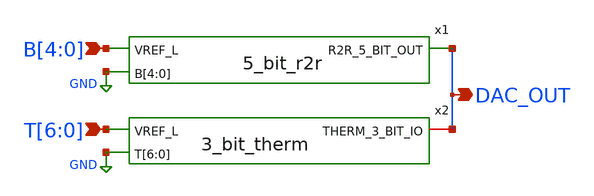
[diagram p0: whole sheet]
** sch_path: xschem/5_3_dac.sch
**.subckt 5_3_dac DAC_OUT B[4],B[3],B[2],B[1],B[0] T[6],T[5],T[4],T[3],T[2],T[1],T[0]
*.opin DAC_OUT
*.ipin B[4],B[3],B[2],B[1],B[0]
*.ipin T[6],T[5],T[4],T[3],T[2],T[1],T[0]
x1 GND GND GND GND GND B[4] DAC_OUT 5_bit_r2r
x2 DAC_OUT T[6] GND GND GND GND GND GND GND 3_bit_therm
**.ends
.GLOBAL GND
.end
